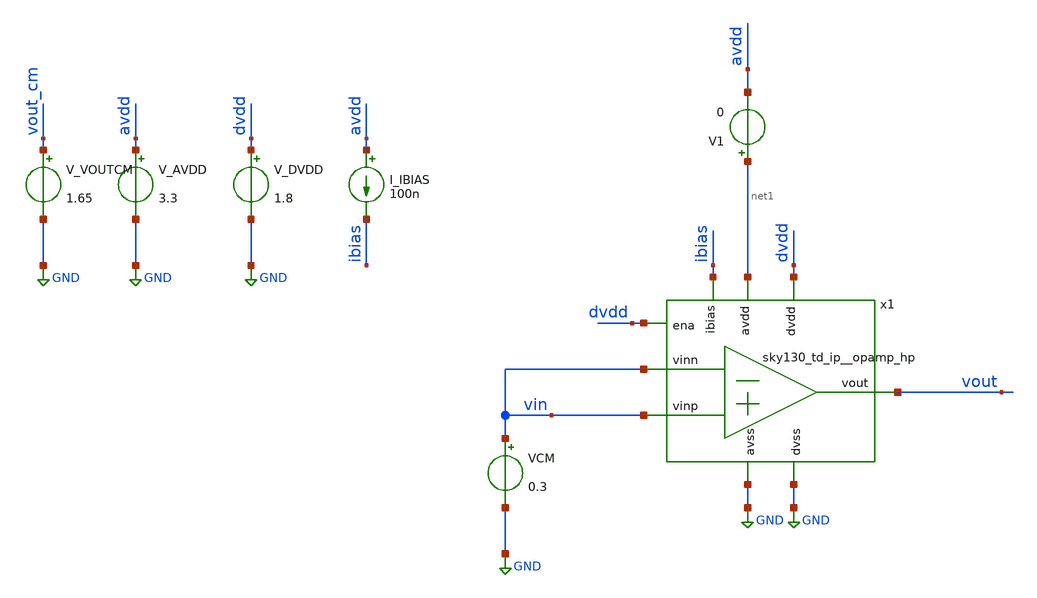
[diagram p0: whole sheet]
** sch_path: xschem/dcpower_noload.sch
**.subckt dcpower_noload
x1 net1 vout ibias vin vin GND dvdd GND dvdd sky130_td_ip__opamp_hp
V_AVDD avdd GND 3.3
.save i(v_avdd)
V_DVDD dvdd GND 1.8
.save i(v_dvdd)
I_IBIAS avdd ibias 100n
V_VOUTCM vout_cm GND 1.65
.save i(v_voutcm)
V1 net1 avdd 0
VCM vin GND 0.3
.save i(vcm)
**** begin user architecture code


.control
save all
alter VCM pwl = [ 0 0 10 3.3 ]
alter VCM dc = 0
tran 10m 10
run
let i_avdd = -1 * i(V1)
meas tran max_iavdd MAX i_avdd

echo Max current from AVDD (no load): $&max_iavdd

plot i_avdd

.endc




.lib /usr/local/share/pdk/sky130A/libs.tech/combined/sky130.lib.spice tt


**** end user architecture code
**.ends
.GLOBAL GND
.end
